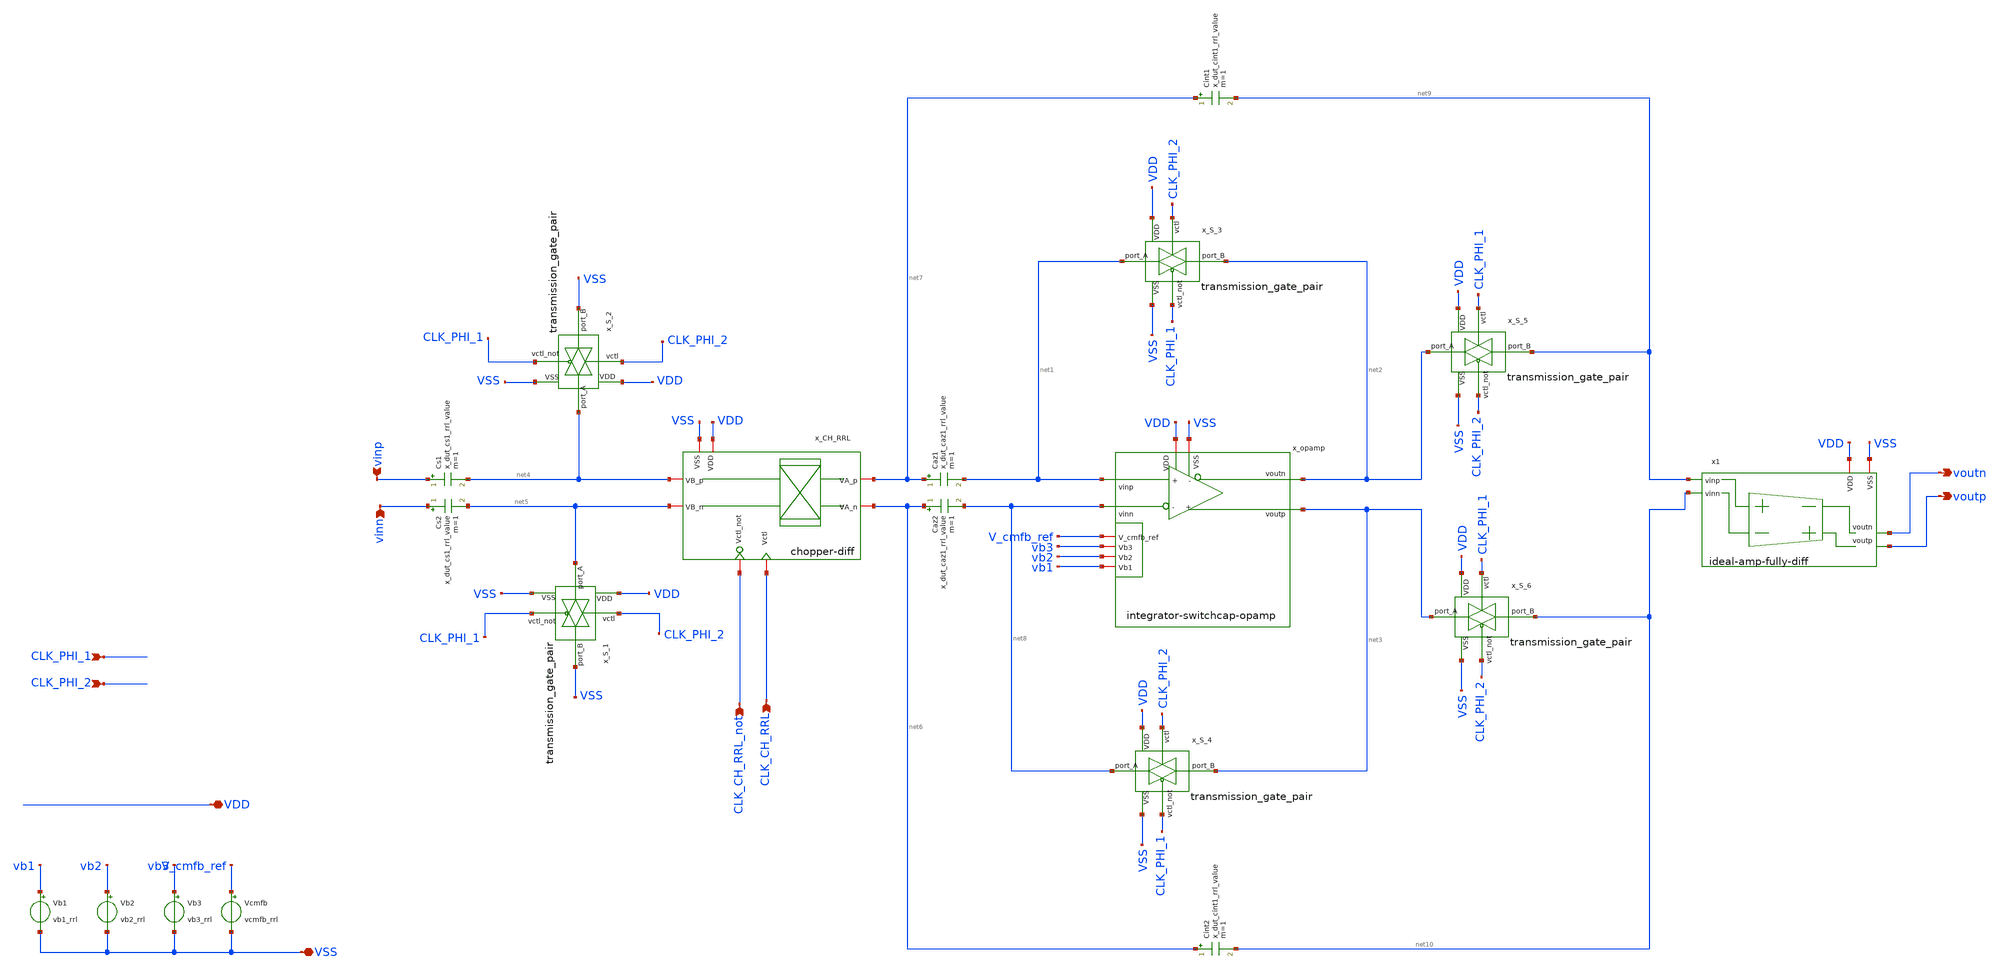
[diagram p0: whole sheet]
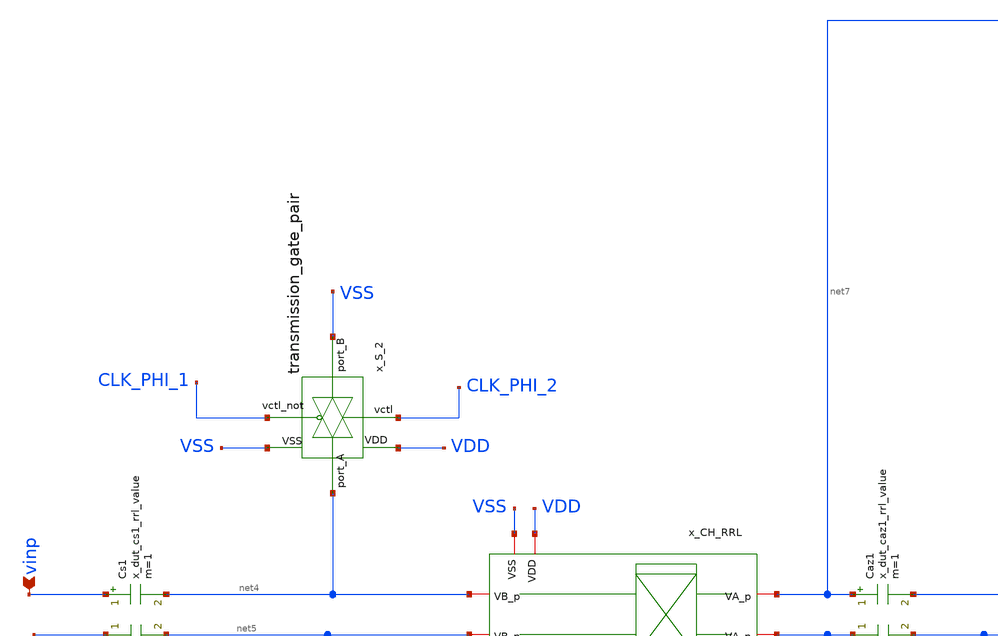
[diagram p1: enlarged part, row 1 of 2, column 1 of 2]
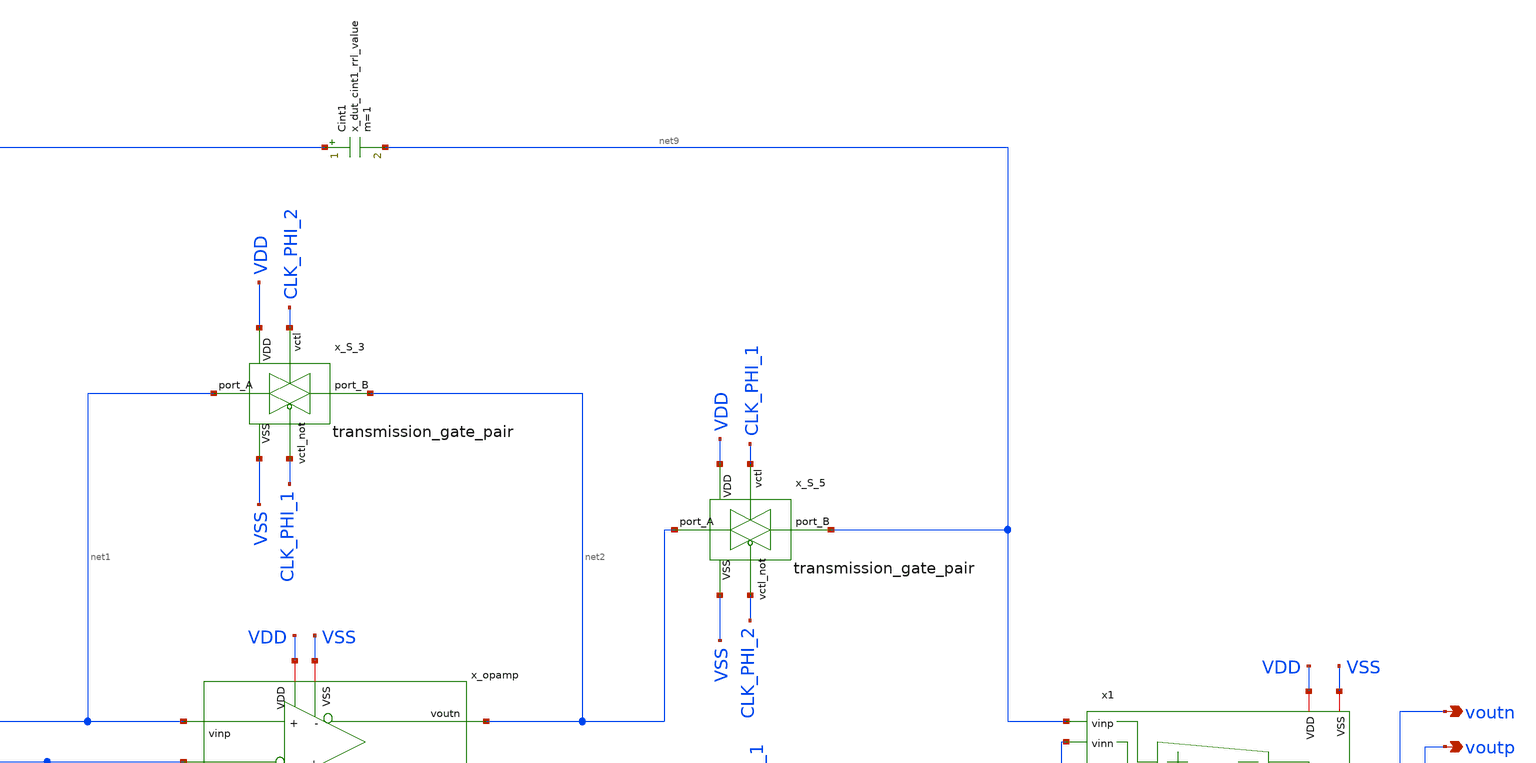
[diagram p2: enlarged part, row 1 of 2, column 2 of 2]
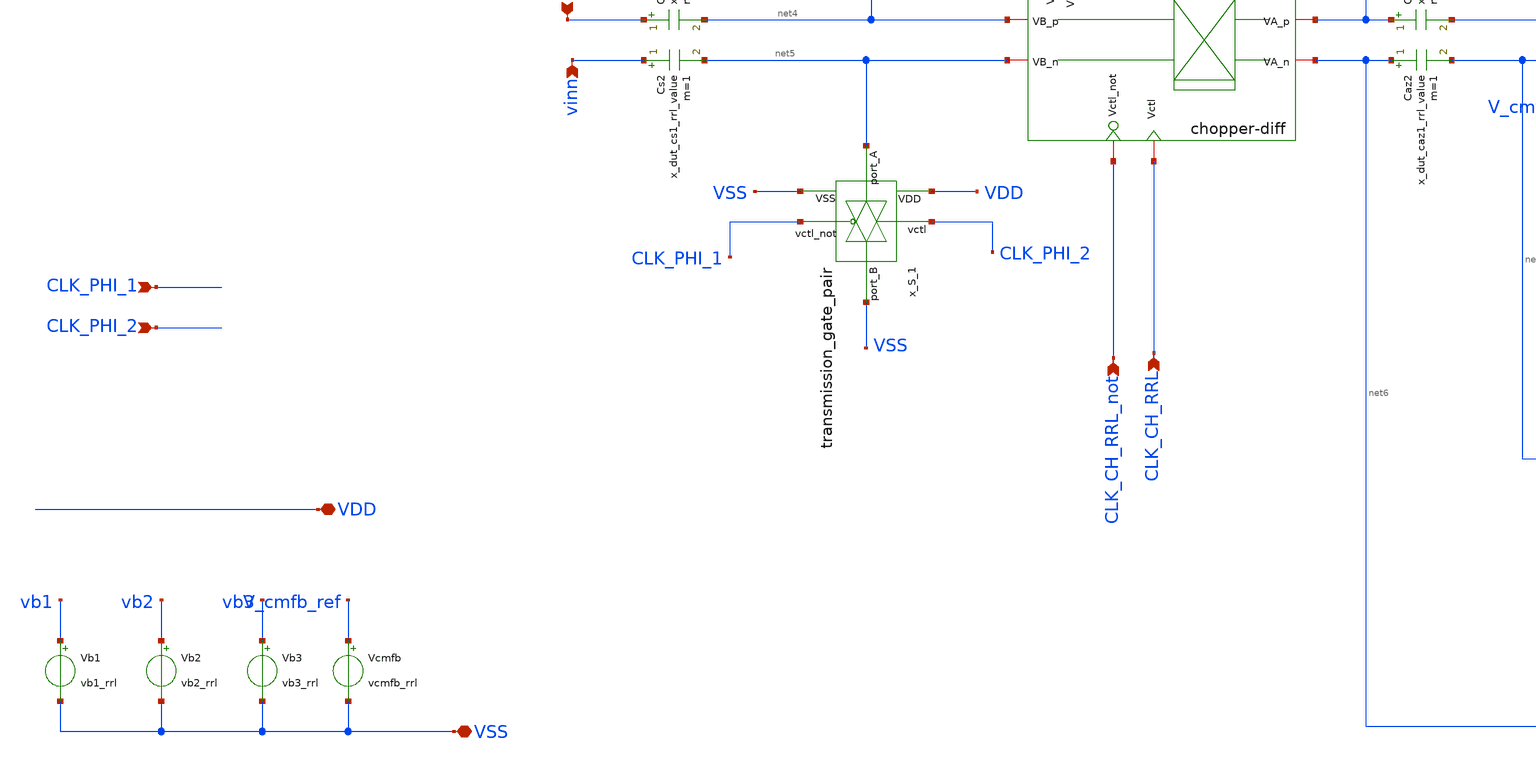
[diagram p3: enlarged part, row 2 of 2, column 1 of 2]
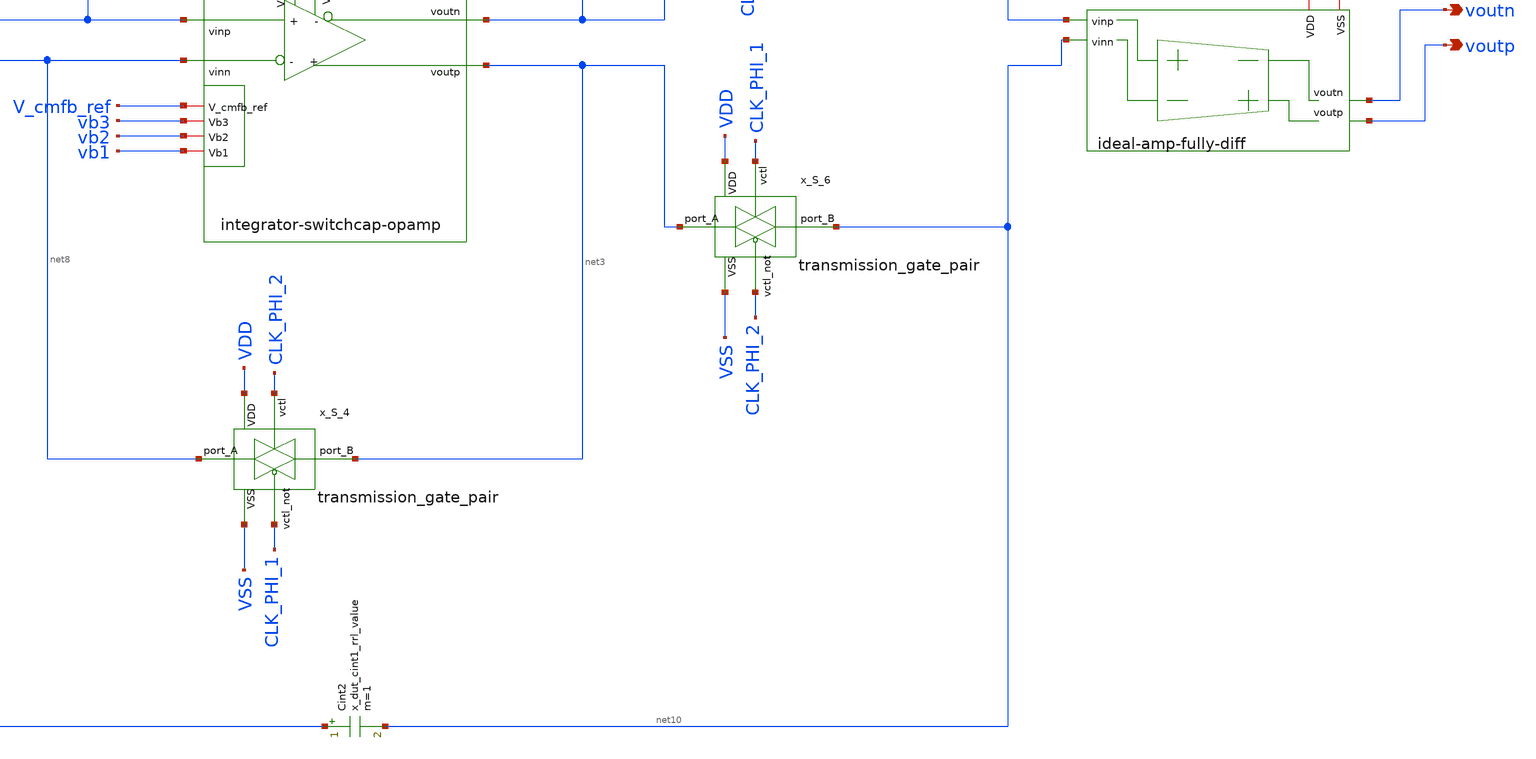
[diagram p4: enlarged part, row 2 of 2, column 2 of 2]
** sch_path: analog-db/drawings/ccia-02-QinwenFan-chopper-ripple-reduction/rrl-switched-capa-integrator.sch
* Copyright 2026 MacAnalog Research Group
**.subckt rrl-switched-capa-integrator VSS VDD vinp vinn CLK_CH_RRL CLK_CH_RRL_not voutn voutp
*+ CLK_PHI_1 CLK_PHI_2
*.iopin VSS
*.iopin VDD
*.ipin vinp
*.ipin vinn
*.ipin CLK_CH_RRL
*.ipin CLK_CH_RRL_not
*.opin voutn
*.opin voutp
*.ipin CLK_PHI_1
*.ipin CLK_PHI_2
x_opamp VDD V_cmfb_ref net8 net2 vb3 net1 vb2 net3 vb1 VSS integrator-switchcap-opamp
Vb1 vb1 VSS vb1_rrl
Vb2 vb2 VSS vb2_rrl
Vb3 vb3 VSS vb3_rrl
Vcmfb V_cmfb_ref VSS vcmfb_rrl
x_CH_RRL CLK_CH_RRL VDD net4 net7 CLK_CH_RRL_not VSS net5 net6 chopper-diff
x_S_2 CLK_PHI_1 VDD VSS VSS net4 CLK_PHI_2 transmission_gate_pair
x_S_1 CLK_PHI_1 VDD VSS VSS net5 CLK_PHI_2 transmission_gate_pair
Cs1 vinp net4 x_dut_cs1_rrl_value m=1
Cs2 vinn net5 x_dut_cs1_rrl_value m=1
Caz1 net7 net1 x_dut_caz1_rrl_value m=1
Caz2 net6 net8 x_dut_caz1_rrl_value m=1
x_S_3 CLK_PHI_1 VDD net2 VSS net1 CLK_PHI_2 transmission_gate_pair
x_S_4 CLK_PHI_1 VDD net3 VSS net8 CLK_PHI_2 transmission_gate_pair
x_S_5 CLK_PHI_2 VDD net9 VSS net2 CLK_PHI_1 transmission_gate_pair
x_S_6 CLK_PHI_2 VDD net10 VSS net3 CLK_PHI_1 transmission_gate_pair
Cint1 net7 net9 x_dut_cint1_rrl_value m=1
Cint2 net6 net10 x_dut_cint1_rrl_value m=1
x1 net9 net10 voutn voutp VSS VDD ideal-amp-fully-diff
**.ends
.end
